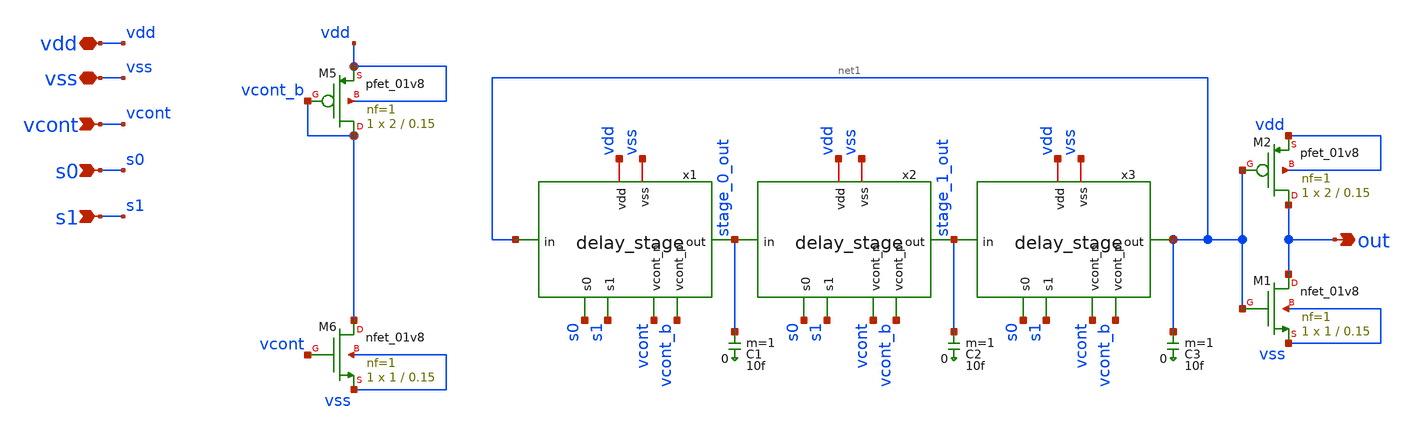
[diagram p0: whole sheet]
** sch_path: xschem/vco.sch
**.subckt vco out vdd s0 s1 vcont vss
*.opin out
*.iopin vdd
*.ipin s0
*.ipin s1
*.ipin vcont
*.iopin vss
x1 vdd vcont_b s0 s1 stage_0_out net1 vcont vss delay_stage
x2 vdd vcont_b s0 s1 stage_1_out stage_0_out vcont vss delay_stage
x3 vdd vcont_b s0 s1 net1 stage_1_out vcont vss delay_stage
C1 stage_0_out 0 10f m=1
C2 stage_1_out 0 10f m=1
C3 net1 0 10f m=1
XM5 vcont_b vcont_b vdd vdd sky130_fd_pr__pfet_01v8 L=0.15 W=2 nf=1 ad='int((nf+1)/2) * W/nf * 0.29'
+ as='int((nf+2)/2) * W/nf * 0.29' pd='2*int((nf+1)/2) * (W/nf + 0.29)' ps='2*int((nf+2)/2) * (W/nf + 0.29)'
+ nrd='0.29 / W' nrs='0.29 / W' sa=0 sb=0 sd=0 mult=1 m=1
XM6 vcont_b vcont vss vss sky130_fd_pr__nfet_01v8 L=0.15 W=1 nf=1 ad='int((nf+1)/2) * W/nf * 0.29' as='int((nf+2)/2) * W/nf * 0.29'
+ pd='2*int((nf+1)/2) * (W/nf + 0.29)' ps='2*int((nf+2)/2) * (W/nf + 0.29)' nrd='0.29 / W' nrs='0.29 / W'
+ sa=0 sb=0 sd=0 mult=1 m=1
XM1 out net1 vss vss sky130_fd_pr__nfet_01v8 L=0.15 W=1 nf=1 ad='int((1 + 1)/2) * 1 / 1 * 0.29' as='int((1 + 2)/2) * 1 / 1 * 0.29'
+ pd='2*int((1 + 1)/2) * (1 / 1 + 0.29)' ps='2*int((1 + 2)/2) * (1 / 1 + 0.29)' nrd='0.29 / 1 ' nrs='0.29 / 1 '
+ sa=0 sb=0 sd=0 mult=1 m=1
XM2 out net1 vdd vdd sky130_fd_pr__pfet_01v8 L=0.15 W=2 nf=1 ad='int((nf+1)/2) * W/nf * 0.29' as='int((nf+2)/2) * W/nf * 0.29'
+ pd='2*int((nf+1)/2) * (W/nf + 0.29)' ps='2*int((nf+2)/2) * (W/nf + 0.29)' nrd='0.29 / W' nrs='0.29 / W'
+ sa=0 sb=0 sd=0 mult=1 m=1
**.ends

* expanding   symbol:  delay_stage.sym # of pins=8
** sym_path: xschem/delay_stage.sym
** sch_path: xschem/delay_stage.sch
.subckt delay_stage vdd vcont_p s0 s1 out in vcont_n vss
*.ipin in
*.opin out
*.iopin vdd
*.ipin vcont_n
*.ipin vcont_p
*.ipin s0
*.ipin s1
*.iopin vss
XM3 out in net2 vss sky130_fd_pr__nfet_01v8 L=0.15 W=1 nf=1 ad='int((nf+1)/2) * W/nf * 0.29' as='int((nf+2)/2) * W/nf * 0.29'
+ pd='2*int((nf+1)/2) * (W/nf + 0.29)' ps='2*int((nf+2)/2) * (W/nf + 0.29)' nrd='0.29 / W' nrs='0.29 / W'
+ sa=0 sb=0 sd=0 mult=1 m=1
XM2 out in net1 vdd sky130_fd_pr__pfet_01v8 L=0.15 W=2 nf=1 ad='int((nf+1)/2) * W/nf * 0.29' as='int((nf+2)/2) * W/nf * 0.29'
+ pd='2*int((nf+1)/2) * (W/nf + 0.29)' ps='2*int((nf+2)/2) * (W/nf + 0.29)' nrd='0.29 / W' nrs='0.29 / W'
+ sa=0 sb=0 sd=0 mult=1 m=1
XM1 net1 vcont_p vdd vdd sky130_fd_pr__pfet_01v8 L=0.15 W=2 nf=1 ad='int((nf+1)/2) * W/nf * 0.29' as='int((nf+2)/2) * W/nf * 0.29'
+ pd='2*int((nf+1)/2) * (W/nf + 0.29)' ps='2*int((nf+2)/2) * (W/nf + 0.29)' nrd='0.29 / W' nrs='0.29 / W'
+ sa=0 sb=0 sd=0 mult=1 m=1
XM4 net2 vcont_n vss vss sky130_fd_pr__nfet_01v8 L=0.15 W=1 nf=1 ad='int((nf+1)/2) * W/nf * 0.29' as='int((nf+2)/2) * W/nf * 0.29'
+ pd='2*int((nf+1)/2) * (W/nf + 0.29)' ps='2*int((nf+2)/2) * (W/nf + 0.29)' nrd='0.29 / W' nrs='0.29 / W'
+ sa=0 sb=0 sd=0 mult=1 m=1
XC2 net3 vss sky130_fd_pr__cap_mim_m3_1 W=2.1 L=2.1 MF=1 m=1
XC1 net4 vss sky130_fd_pr__cap_mim_m3_1 W=2.1 L=4.2 MF=1 m=1
XM5 out s0 net4 vss sky130_fd_pr__nfet_01v8 L=0.15 W=1 nf=1 ad='int((nf+1)/2) * W/nf * 0.29' as='int((nf+2)/2) * W/nf * 0.29'
+ pd='2*int((nf+1)/2) * (W/nf + 0.29)' ps='2*int((nf+2)/2) * (W/nf + 0.29)' nrd='0.29 / W' nrs='0.29 / W'
+ sa=0 sb=0 sd=0 mult=1 m=1
XM6 out s1 net3 vss sky130_fd_pr__nfet_01v8 L=0.15 W=1 nf=1 ad='int((nf+1)/2) * W/nf * 0.29' as='int((nf+2)/2) * W/nf * 0.29'
+ pd='2*int((nf+1)/2) * (W/nf + 0.29)' ps='2*int((nf+2)/2) * (W/nf + 0.29)' nrd='0.29 / W' nrs='0.29 / W'
+ sa=0 sb=0 sd=0 mult=1 m=1
.ends

.end
